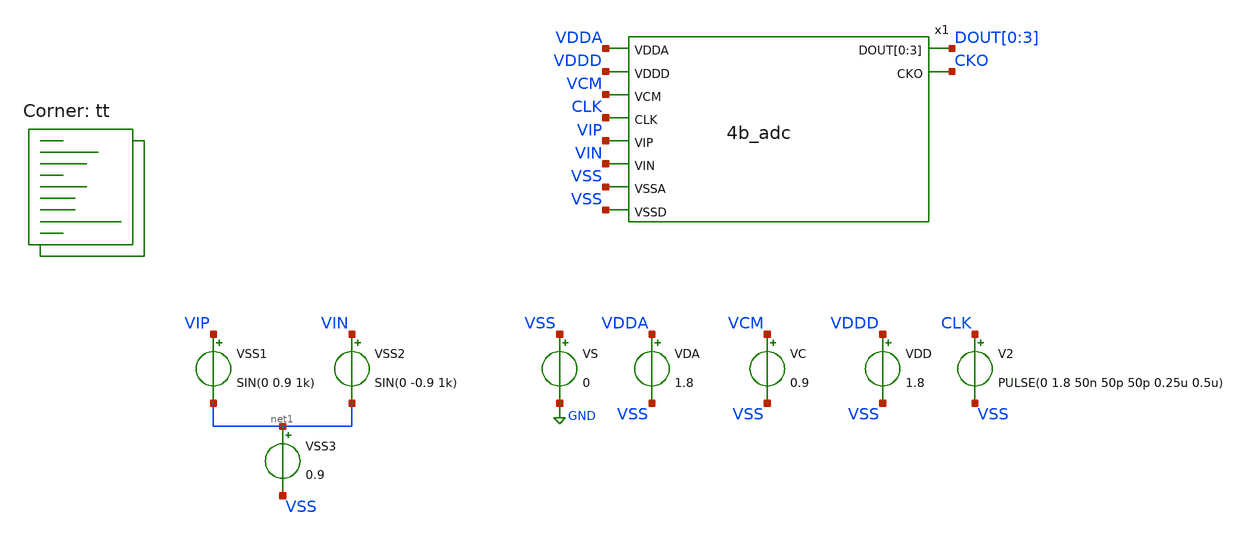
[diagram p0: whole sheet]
** sch_path: xschem/adc_tb.sch
**.subckt adc_tb
x1 VDDA VDDD VCM CLK VIP VIN VSS VSS DOUT[0] DOUT[1] DOUT[2] DOUT[3] CKO 4b_adc
VS VSS GND 0
VDA VDDA VSS 1.8
VDD VDDD VSS 1.8
VC VCM VSS 0.9
VSS1 VIP net1 SIN(0 0.9 1k)
VSS2 VIN net1 SIN(0 -0.9 1k)
VSS3 net1 VSS 0.9
V2 CLK VSS PULSE(0 1.8 50n 50p 50p 0.25u 0.5u)
**** begin user architecture code

** opencircuitdesign pdks install
* .lib $::SKYWATER_MODELS/sky130.lib.spice tt
.include /usr/local/share/pdk/sky130A/libs.ref/sky130_fd_sc_hd/spice/sky130_fd_sc_hd.spice



.option wnflag=0
.option savecurrents
.options acct list
.options method=gear
.control
global netlist_dir .
set wr_singlescale
save  x1.vcp  x1.vcn  cko
tran 100n 2m uic
plot x1.vcp x1.vcn
plot cko
wrdata output.txt  x1.vcp  x1.vcn  cko
.endc

.lib $::SKYWATER_MODELS/sky130.lib.spice tt
**** end user architecture code
**.ends
.GLOBAL GND
.end
